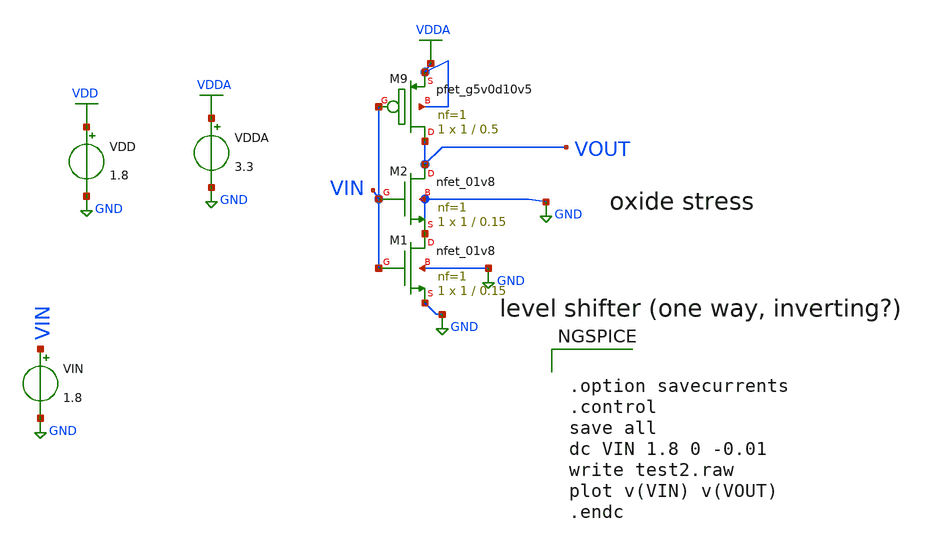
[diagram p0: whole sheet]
** sch_path: xschem/lthlogicshifter.sch
**.subckt lthlogicshifter
VDD VDD GND 1.8
VIN VIN GND 1.8
VDDA VDDA GND 3.3
XM9 VOUT VIN VDDA VDDA sky130_fd_pr__pfet_g5v0d10v5 L=0.5 W=1 nf=1 ad='int((1 + 1)/2) * 1 / 1 * 0.29'
+ as='int((1 + 2)/2) * 1 / 1 * 0.29' pd='2*int((1 + 1)/2) * (1 / 1 + 0.29)' ps='2*int((1 + 2)/2) * (1 / 1 + 0.29)'
+ nrd='0.29 / 1 ' nrs='0.29 / 1 ' sa=0 sb=0 sd=0 mult=1 m=1
XM2 VOUT VIN GND GND sky130_fd_pr__nfet_01v8 L=0.15 W=1 nf=1 ad='int((1 + 1)/2) * 1 / 1 * 0.29' as='int((1 + 2)/2) * 1 / 1 * 0.29'
+ pd='2*int((1 + 1)/2) * (1 / 1 + 0.29)' ps='2*int((1 + 2)/2) * (1 / 1 + 0.29)' nrd='0.29 / 1 ' nrs='0.29 / 1 '
+ sa=0 sb=0 sd=0 mult=1 m=1
XM1 GND VIN GND GND sky130_fd_pr__nfet_01v8 L=0.15 W=1 nf=1 ad='int((1 + 1)/2) * 1 / 1 * 0.29' as='int((1 + 2)/2) * 1 / 1 * 0.29'
+ pd='2*int((1 + 1)/2) * (1 / 1 + 0.29)' ps='2*int((1 + 2)/2) * (1 / 1 + 0.29)' nrd='0.29 / 1 ' nrs='0.29 / 1 '
+ sa=0 sb=0 sd=0 mult=1 m=1
**** begin user architecture code

** opencircuitdesign pdks install
.lib $::SKYWATER_MODELS/sky130.lib.spice tt




.option savecurrents
.control
save all
dc VIN 1.8 0 -0.01
write test2.raw
plot v(VIN) v(VOUT)
.endc


**** end user architecture code
**.ends
.GLOBAL GND
.GLOBAL VDD
.GLOBAL VDDA
.end
